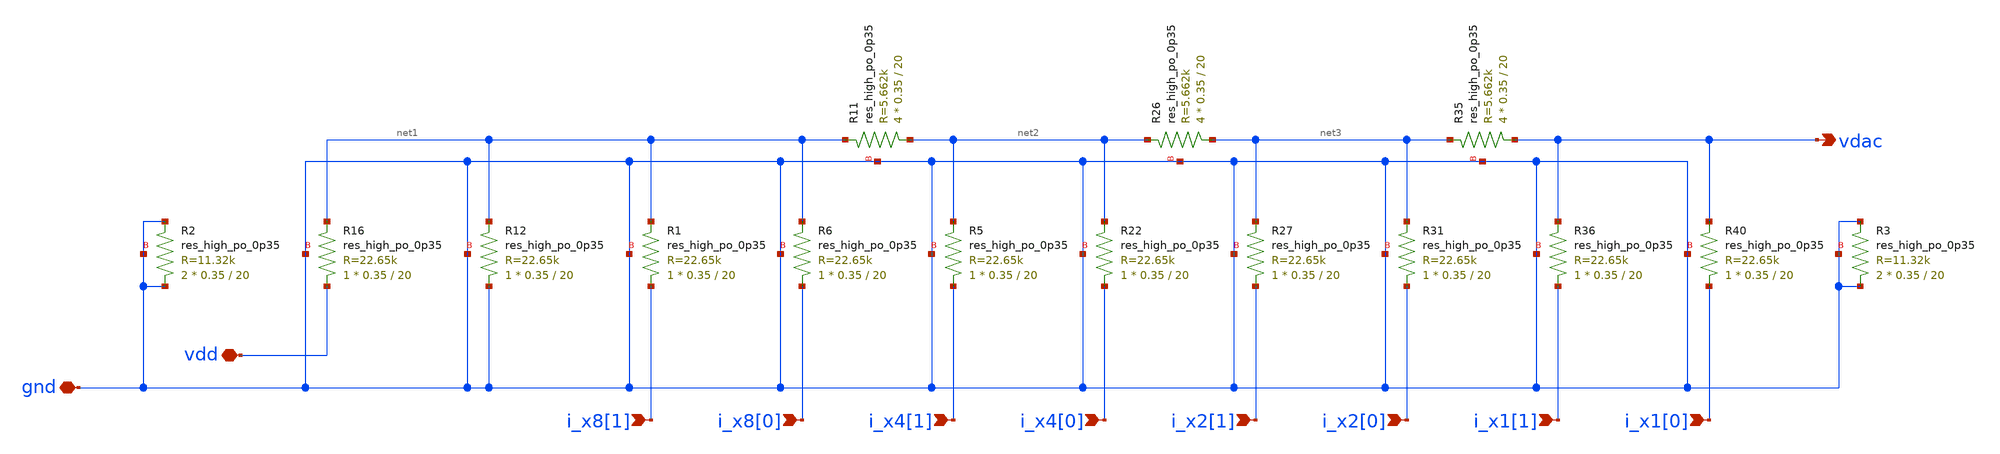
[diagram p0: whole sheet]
** sch_path: xschem/ef_smsdac8_ladder.sch
**.subckt ef_smsdac8_ladder vdd vdac i_x8[1] gnd i_x8[0] i_x4[1] i_x4[0] i_x2[1] i_x2[0] i_x1[1]
*+ i_x1[0]
*.iopin vdd
*.opin vdac
*.ipin i_x8[1]
*.iopin gnd
*.ipin i_x8[0]
*.ipin i_x4[1]
*.ipin i_x4[0]
*.ipin i_x2[1]
*.ipin i_x2[0]
*.ipin i_x1[1]
*.ipin i_x1[0]
XR1 i_x8[1] net1 gnd sky130_fd_pr__res_high_po_0p35 L=20 mult=1 m=1
XR6 i_x8[0] net1 gnd sky130_fd_pr__res_high_po_0p35 L=20 mult=1 m=1
XR11 net2 net1 gnd sky130_fd_pr__res_high_po_0p35 L=20 mult=4 m=4
XR12 gnd net1 gnd sky130_fd_pr__res_high_po_0p35 L=20 mult=1 m=1
XR16 vdd net1 gnd sky130_fd_pr__res_high_po_0p35 L=20 mult=1 m=1
XR5 i_x4[1] net2 gnd sky130_fd_pr__res_high_po_0p35 L=20 mult=1 m=1
XR22 i_x4[0] net2 gnd sky130_fd_pr__res_high_po_0p35 L=20 mult=1 m=1
XR26 net3 net2 gnd sky130_fd_pr__res_high_po_0p35 L=20 mult=4 m=4
XR27 i_x2[1] net3 gnd sky130_fd_pr__res_high_po_0p35 L=20 mult=1 m=1
XR31 i_x2[0] net3 gnd sky130_fd_pr__res_high_po_0p35 L=20 mult=1 m=1
XR35 vdac net3 gnd sky130_fd_pr__res_high_po_0p35 L=20 mult=4 m=4
XR36 i_x1[1] vdac gnd sky130_fd_pr__res_high_po_0p35 L=20 mult=1 m=1
XR40 i_x1[0] vdac gnd sky130_fd_pr__res_high_po_0p35 L=20 mult=1 m=1
XR2 gnd gnd gnd sky130_fd_pr__res_high_po_0p35 L=20 mult=2 m=2
XR3 gnd gnd gnd sky130_fd_pr__res_high_po_0p35 L=20 mult=2 m=2
**.ends
.end
